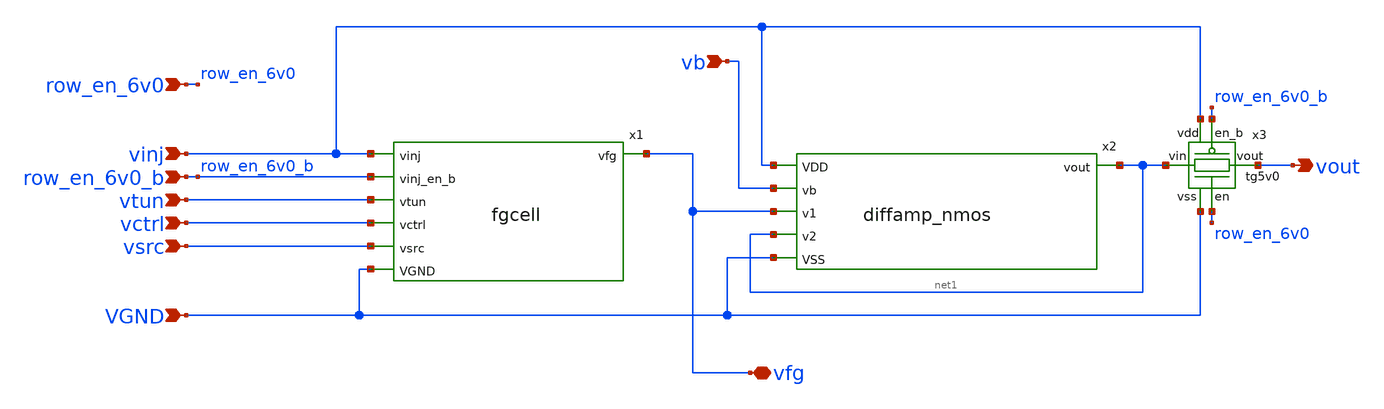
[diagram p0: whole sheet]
** sch_path: xschem/fgcell_amp.sch
**.subckt fgcell_amp vinj row_en_6v0_b vtun vctrl vsrc vb VGND vout vfg row_en_6v0
*.ipin vinj
*.ipin row_en_6v0_b
*.ipin vtun
*.ipin vctrl
*.ipin vsrc
*.ipin vb
*.ipin VGND
*.opin vout
*.iopin vfg
*.ipin row_en_6v0
x1 vinj row_en_6v0_b vtun vctrl vsrc VGND vfg fgcell
x2 vfg net1 vb net1 vinj VGND diffamp_nmos
x3 net1 vout row_en_6v0 row_en_6v0_b vinj VGND tg5v0
**.ends
.end
